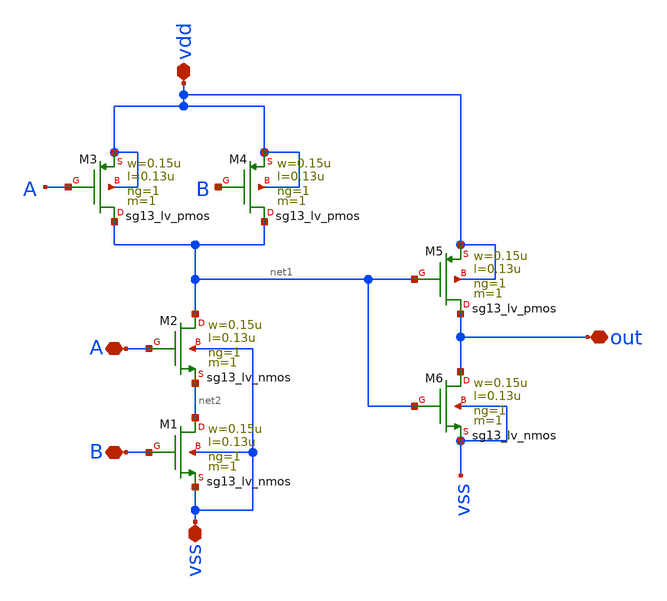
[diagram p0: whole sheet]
** sch_path: design/blocks/puertaand/puertaand.sch
**.subckt puertaand A B vdd vss out
*.iopin A
*.iopin B
*.iopin vdd
*.iopin vss
*.iopin out
XM1 net2 B vss vss sg13_lv_nmos w=0.15u l=0.13u ng=1 m=1 mm_ok=1
XM2 net1 A net2 vss sg13_lv_nmos w=0.15u l=0.13u ng=1 m=1 mm_ok=1
XM3 net1 A vdd vdd sg13_lv_pmos w=0.15u l=0.13u ng=1 m=1 mm_ok=1
XM4 net1 B vdd vdd sg13_lv_pmos w=0.15u l=0.13u ng=1 m=1 mm_ok=1
XM5 out net1 vdd vdd sg13_lv_pmos w=0.15u l=0.13u ng=1 m=1 mm_ok=1
XM6 out net1 vss vss sg13_lv_nmos w=0.15u l=0.13u ng=1 m=1 mm_ok=1
**.ends
.end
